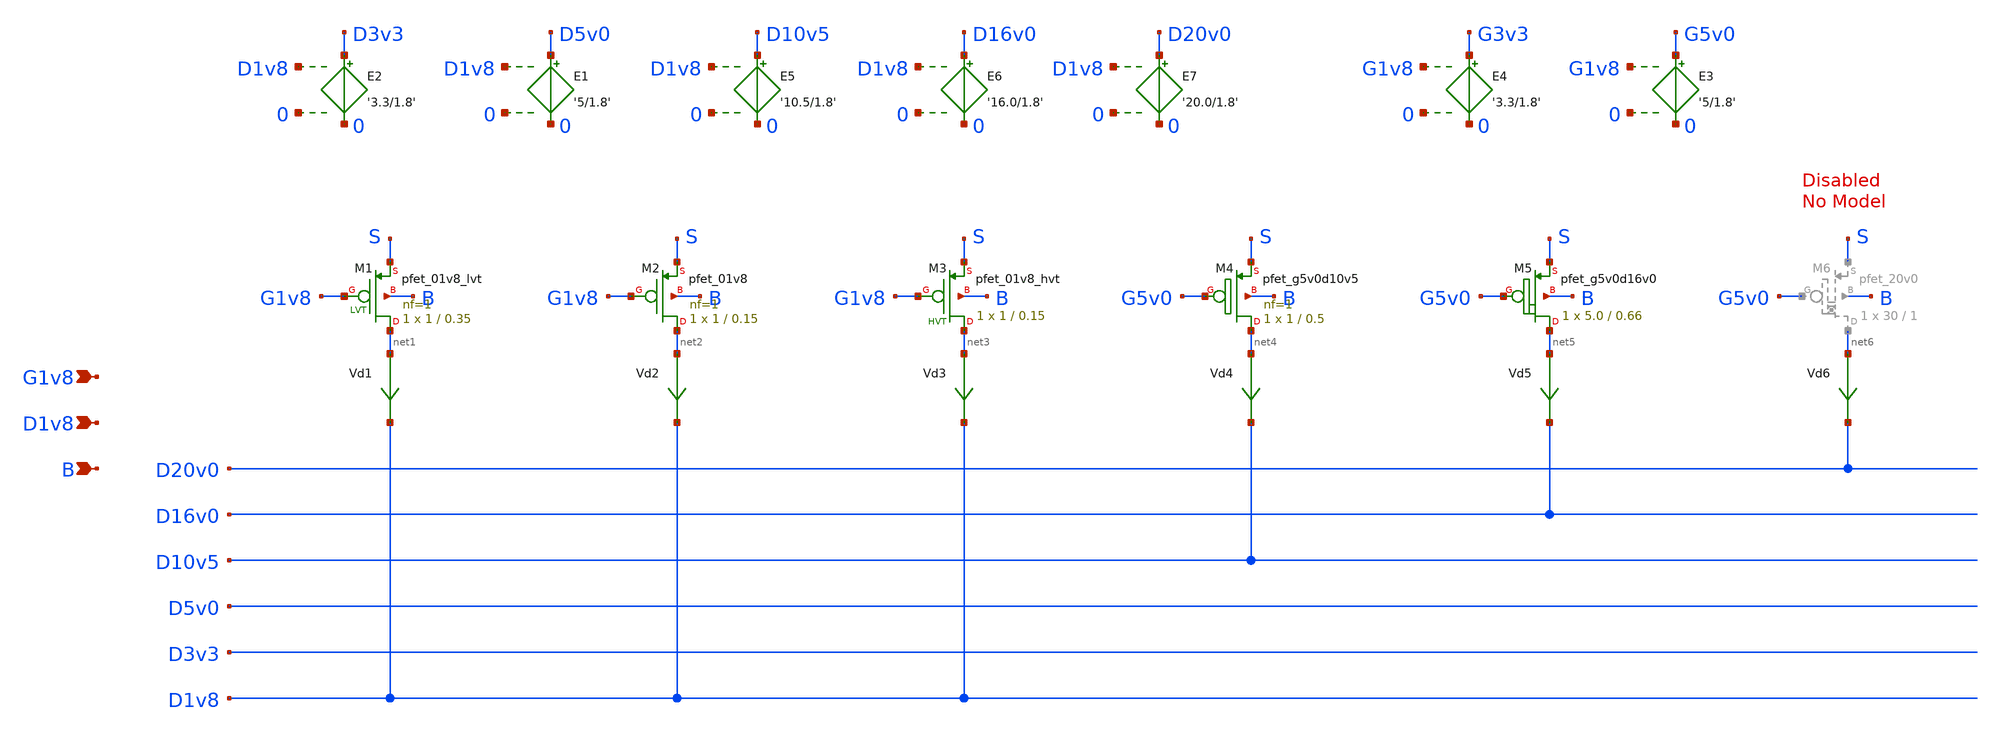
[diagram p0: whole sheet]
** sch_path: sky130_tests/test_pmos.sch
* Copyright 2020 Stefan Frederik Schippers
* Licensed under the Apache License, Version 2.0 (the "License");
* you may not use this file except in compliance with the License.
* You may obtain a copy of the License at
* https://www.apache.org/licenses/LICENSE-2.0
* Unless required by applicable law or agreed to in writing, software
* distributed under the License is distributed on an "AS IS" BASIS,
* WITHOUT WARRANTIES OR CONDITIONS OF ANY KIND, either express or implied.
* See the License for the specific language governing permissions and
* limitations under the License.
**.subckt test_pmos G1v8 D1v8 B
*.ipin G1v8
*.ipin D1v8
*.ipin B
Vd1 net1 D1v8 0
.save i(vd1)
Vd2 net2 D1v8 0
.save i(vd2)
E1 D5v0 0 D1v8 0 '5/1.8'
E2 D3v3 0 D1v8 0 '3.3/1.8'
E3 G5v0 0 G1v8 0 '5/1.8'
E4 G3v3 0 G1v8 0 '3.3/1.8'
E5 D10v5 0 D1v8 0 '10.5/1.8'
Vd3 net3 D1v8 0
.save i(vd3)
XM3 net3 G1v8 S B sky130_fd_pr__pfet_01v8_hvt W=1 L=0.15 ad='W * 0.29' pd='W + 2 * 0.29' as='W * 0.29'
+ ps='W + 2 * 0.29' nrd=0 nrs=0 sa=0 sb=0 sd=0 nf=1 mult=1
Vd4 net4 D10v5 0
.save i(vd4)
XM4 net4 G5v0 S B sky130_fd_pr__pfet_g5v0d10v5 L=0.5 W=1 nf=1 ad='W * 0.29' as='W * 0.29' pd='W + 2 * 0.29'
+ ps='W + 2 * 0.29' nrd=0 nrs=0 sa=0 sb=0 sd=0 mult=1 m=1
XM1 net1 G1v8 S B sky130_fd_pr__pfet_01v8_lvt L=0.35 W=1 nf=1 ad='W * 0.29' as='W * 0.29' pd='W + 2 * 0.29'
+ ps='W + 2 * 0.29' nrd=0 nrs=0 sa=0 sb=0 sd=0 mult=1 m=1
XM2 net2 G1v8 S B sky130_fd_pr__pfet_01v8 L=0.15 W=1 nf=1 ad='W * 0.29' as='W * 0.29' pd='W + 2 * 0.29'
+ ps='W + 2 * 0.29' nrd=0 nrs=0 sa=0 sb=0 sd=0 mult=1 m=1
Vd5 net5 D16v0 0
.save i(vd5)
XM5 net5 G5v0 S B sky130_fd_pr__pfet_g5v0d16v0 W=5.0 L=0.66 ad='W * 0.29' pd='W + 2 * 0.29' as='W * 0.29'
+ ps='W + 2 * 0.29' nrd=0 nrs=0 sa=0 sb=0 sd=0 nf=1 mult=1 m=1
E6 D16v0 0 D1v8 0 '16.0/1.8'
E7 D20v0 0 D1v8 0 '20.0/1.8'
Vd6 net6 D20v0 0
.save i(vd6)
**** begin user architecture code


* .lib "~/skywater-pdk/sky130_fd_pr/models/sky130.lib.spice" tt

* temporary fix: some model equations use temp instead of the true
* ngspice temperature variable, 'temper'
.param temp=27

vg G1v8 0 0
vs s 0 0
vd D1v8 0 0
vb b 0 0
.control
dc vd 0 -1.8 -0.01 vg 0 -1.8 -0.2
plot all.vd1#branch vs D1v8
plot all.vd2#branch vs D1v8
plot all.vd3#branch vs D1v8
plot all.vd4#branch vs D10v5
plot all.vd5#branch vs D16v0

.endc


**** end user architecture code
**.ends
**** begin user architecture code

.include   ~/skywater-pdk/sky130_fd_pr_ngspice/cells/nfet_01v8/sky130_fd_pr__nfet_01v8__tt.corner.spice
.include ~/skywater-pdk/sky130_fd_pr_ngspice/cells/nfet_01v8_lvt/sky130_fd_pr__nfet_01v8_lvt__tt.corner.spice
.include ~/skywater-pdk/sky130_fd_pr_ngspice/cells/pfet_01v8/sky130_fd_pr__pfet_01v8__tt.corner.spice
.include ~/skywater-pdk/sky130_fd_pr_ngspice/cells/nfet_03v3_nvt/sky130_fd_pr__nfet_03v3_nvt__tt.corner.spice
.include ~/skywater-pdk/sky130_fd_pr_ngspice/cells/nfet_05v0_nvt/sky130_fd_pr__nfet_05v0_nvt__tt.corner.spice
.include ~/skywater-pdk/sky130_fd_pr_ngspice/cells/esd_nfet_01v8/sky130_fd_pr__esd_nfet_01v8__tt.corner.spice
.include ~/skywater-pdk/sky130_fd_pr_ngspice/cells/pfet_01v8_lvt/sky130_fd_pr__pfet_01v8_lvt__tt.corner.spice
.include ~/skywater-pdk/sky130_fd_pr_ngspice/cells/pfet_01v8_hvt/sky130_fd_pr__pfet_01v8_hvt__tt.corner.spice
.include ~/skywater-pdk/sky130_fd_pr_ngspice/cells/esd_pfet_g5v0d10v5/sky130_fd_pr__esd_pfet_g5v0d10v5__tt.corner.spice
.include ~/skywater-pdk/sky130_fd_pr_ngspice/cells/pfet_g5v0d10v5/sky130_fd_pr__pfet_g5v0d10v5__tt.corner.spice
.include ~/skywater-pdk/sky130_fd_pr_ngspice/cells/pfet_g5v0d16v0/sky130_fd_pr__pfet_g5v0d16v0__tt.corner.spice
.include ~/skywater-pdk/sky130_fd_pr_ngspice/cells/nfet_g5v0d10v5/sky130_fd_pr__nfet_g5v0d10v5__tt.corner.spice
.include ~/skywater-pdk/sky130_fd_pr_ngspice/cells/nfet_g5v0d16v0/sky130_fd_pr__nfet_g5v0d16v0__tt_discrete.corner.spice
.include ~/skywater-pdk/sky130_fd_pr_ngspice/cells/esd_nfet_g5v0d10v5/sky130_fd_pr__esd_nfet_g5v0d10v5__tt.corner.spice
.include ~/skywater-pdk/sky130_fd_pr_ngspice/models/corners/tt/nonfet.spice
* Mismatch parameters
.include ~/skywater-pdk/sky130_fd_pr_ngspice/cells/nfet_01v8/sky130_fd_pr__nfet_01v8__mismatch.corner.spice
.include ~/skywater-pdk/sky130_fd_pr_ngspice/cells/pfet_01v8/sky130_fd_pr__pfet_01v8__mismatch.corner.spice
.include ~/skywater-pdk/sky130_fd_pr_ngspice/cells/nfet_01v8_lvt/sky130_fd_pr__nfet_01v8_lvt__mismatch.corner.spice
.include ~/skywater-pdk/sky130_fd_pr_ngspice/cells/pfet_01v8_lvt/sky130_fd_pr__pfet_01v8_lvt__mismatch.corner.spice
.include ~/skywater-pdk/sky130_fd_pr_ngspice/cells/pfet_01v8_hvt/sky130_fd_pr__pfet_01v8_hvt__mismatch.corner.spice
.include ~/skywater-pdk/sky130_fd_pr_ngspice/cells/nfet_g5v0d10v5/sky130_fd_pr__nfet_g5v0d10v5__mismatch.corner.spice
.include ~/skywater-pdk/sky130_fd_pr_ngspice/cells/pfet_g5v0d10v5/sky130_fd_pr__pfet_g5v0d10v5__mismatch.corner.spice
.include ~/skywater-pdk/sky130_fd_pr_ngspice/cells/nfet_05v0_nvt/sky130_fd_pr__nfet_05v0_nvt__mismatch.corner.spice
.include ~/skywater-pdk/sky130_fd_pr_ngspice/cells/nfet_03v3_nvt/sky130_fd_pr__nfet_03v3_nvt__mismatch.corner.spice
* Resistor/Capacitor
.include ~/skywater-pdk/sky130_fd_pr_ngspice/models/r+c/res_typical__cap_typical.spice
.include ~/skywater-pdk/sky130_fd_pr_ngspice/models/r+c/res_typical__cap_typical__lin.spice
* Special cells
.include ~/skywater-pdk/sky130_fd_pr_ngspice/models/corners/tt/specialized_cells.spice
* All models
.include ~/skywater-pdk/sky130_fd_pr_ngspice/models/all.spice
* Corner
.include ~/skywater-pdk/sky130_fd_pr_ngspice/models/corners/tt/rf.spice


**** end user architecture code
.end
